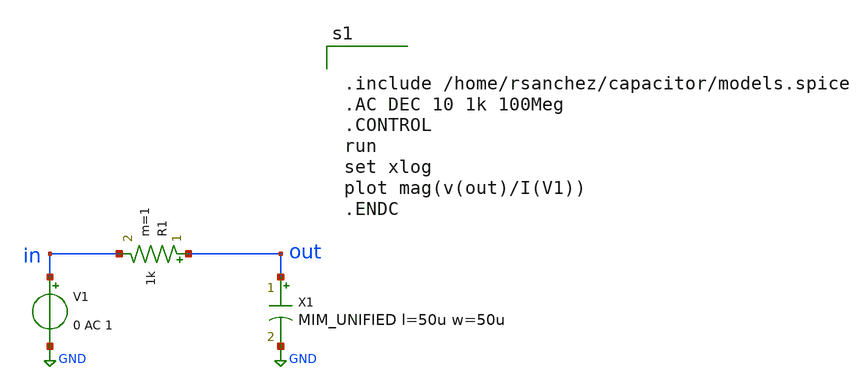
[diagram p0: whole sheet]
** sch_path: _legacy/capacitor/capacitor/cap_test.sch
**.subckt cap_test
X1 out GND MIM_UNIFIED l=50u w=50u m=
R1 out in 1k m=1
V1 in GND 0 AC 1
**** begin user architecture code


.include /home/rsanchez/capacitor/models.spice
.AC DEC 10 1k 100Meg
.CONTROL
run
set xlog
plot mag(v(out)/I(V1))
.ENDC


**** end user architecture code
**.ends
.GLOBAL GND
.end
